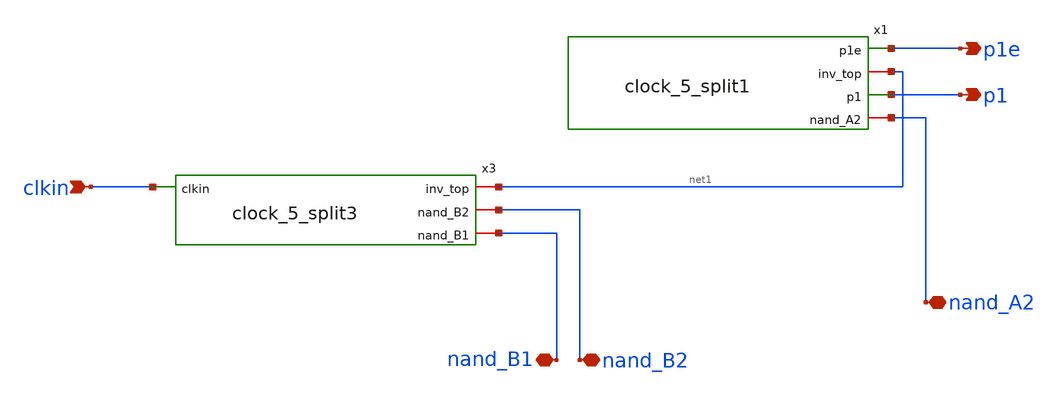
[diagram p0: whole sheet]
** sch_path: 5_Design/4_Layout/Team 5/xschem/clock_5_splitTop1.sch
* IHP-GmbH/IHP-Open-PDK/ihp-sg13g2/libs.tech/xschem/sg13g2_stdcells/sg13g2_inv_2.sch:
* Copyright 2023 IHP PDK Authors
* Licensed under the Apache License, Version 2.0 (the "License");
**.subckt clock_5_splitTop1 clkin p1e p1 nand_B2 nand_B1 nand_A2
*.ipin clkin
*.opin p1e
*.opin p1
*.iopin nand_B2
*.iopin nand_B1
*.iopin nand_A2
x1 p1e net1 p1 nand_A2 clock_5_split1
x3 net1 clkin nand_B2 nand_B1 clock_5_split3
**.ends

* expanding   symbol:  /foss/designs/clock_5_split1.sym # of pins=4
** sym_path: 5_Design/4_Layout/Team 5/xschem/clock_5_split1.sym
** sch_path: 5_Design/4_Layout/Team 5/xschem/clock_5_split1.sch
.subckt clock_5_split1 p1e inv_top p1 nand_A2
*.opin p1e
*.opin p1
*.iopin inv_top
*.iopin nand_A2
x7 a1 inv_top VDD VSS sg13g2_inv_4
x8 p1e a1 VDD VSS sg13g2_inv_4
x9 nand_A2 p1e VDD VSS sg13g2_inv_4
x11 net2 net1 VDD VSS sg13g2_inv_4
x3 p1 net2 VDD VSS sg13g2_inv_8
x14 net1 a1 nand_A2 VDD VSS sg13g2_nand2_2
.ends


* expanding   symbol:  /foss/designs/clock_5_split3.sym # of pins=4
** sym_path: 5_Design/4_Layout/Team 5/splitUpSimulationsAndSchematics/clock_5_split3.sym
** sch_path: 5_Design/4_Layout/Team 5/splitUpSimulationsAndSchematics/clock_5_split3.sch
.subckt clock_5_split3 inv_top clkin nand_B2 nand_B1
*.ipin clkin
*.iopin nand_B2
*.iopin nand_B1
*.iopin inv_top
x4 net2 net1 VDD VSS sg13g2_inv_4
x5 net3 net2 VDD VSS sg13g2_inv_4
x6 inv_top net3 VDD VSS sg13g2_inv_4
x13 nand_B2 clkin VDD VSS sg13g2_inv_2
x1 clkinbb nand_B2 VDD VSS sg13g2_inv_2
x2 net1 nand_B1 clkinbb VDD VSS sg13g2_nand2_2
.ends


* expanding   symbol:  sg13g2_stdcells/sg13g2_inv_4.sym # of pins=2
** sym_path: sg13g2_stdcells/sg13g2_inv_4.sym
** sch_path: sg13g2_stdcells/sg13g2_inv_4.sch
.subckt sg13g2_inv_4 Y A VDD VSS
*.ipin A
*.opin Y
*.iopin VDD
*.iopin VSS
XM1 Y A VSS VSS sg13_lv_nmos w=2.96u l=130.00n ng=4 m=1 mm_ok=1
XM2 Y A VDD VDD sg13_lv_pmos w=4.48u l=130.00n ng=4 m=1 mm_ok=1
.ends


* expanding   symbol:  sg13g2_stdcells/sg13g2_inv_8.sym # of pins=2
** sym_path: sg13g2_stdcells/sg13g2_inv_8.sym
** sch_path: sg13g2_stdcells/sg13g2_inv_8.sch
.subckt sg13g2_inv_8 Y A VDD VSS
*.opin Y
*.ipin A
*.iopin VDD
*.iopin VSS
XM1 Y A VSS VSS sg13_lv_nmos w=5.92u l=130.00n ng=8 m=1 mm_ok=1
XM2 Y A VDD VDD sg13_lv_pmos w=8.96u l=130.00n ng=8 m=1 mm_ok=1
.ends


* expanding   symbol:  sg13g2_stdcells/sg13g2_nand2_2.sym # of pins=3
** sym_path: sg13g2_stdcells/sg13g2_nand2_2.sym
** sch_path: sg13g2_stdcells/sg13g2_nand2_2.sch
.subckt sg13g2_nand2_2 Y A B VDD VSS
*.iopin VDD
*.iopin VSS
*.opin Y
*.ipin B
*.ipin A
XM1 Y A net1 VSS sg13_lv_nmos w=1.44u l=130.00n ng=2 m=1 mm_ok=1
XM2 net1 B VSS VSS sg13_lv_nmos w=1.44u l=130.00n ng=2 m=1 mm_ok=1
XM3 Y A VDD VDD sg13_lv_pmos w=2.24u l=130.00n ng=2 m=1 mm_ok=1
XM4 Y B VDD VDD sg13_lv_pmos w=2.24u l=130.00n ng=2 m=1 mm_ok=1
.ends


* expanding   symbol:  sg13g2_stdcells/sg13g2_inv_2.sym # of pins=2
** sym_path: sg13g2_stdcells/sg13g2_inv_2.sym
** sch_path: sg13g2_stdcells/sg13g2_inv_2.sch
.subckt sg13g2_inv_2 Y A VDD VSS
*.opin Y
*.ipin A
*.iopin VDD
*.iopin VSS
XM1 Y A VSS VSS sg13_lv_nmos w=1.48u l=130.00n ng=2 m=1 mm_ok=1
XM2 Y A VDD VDD sg13_lv_pmos w=2.24u l=130.00n ng=2 m=1 mm_ok=1
.ends

.end
